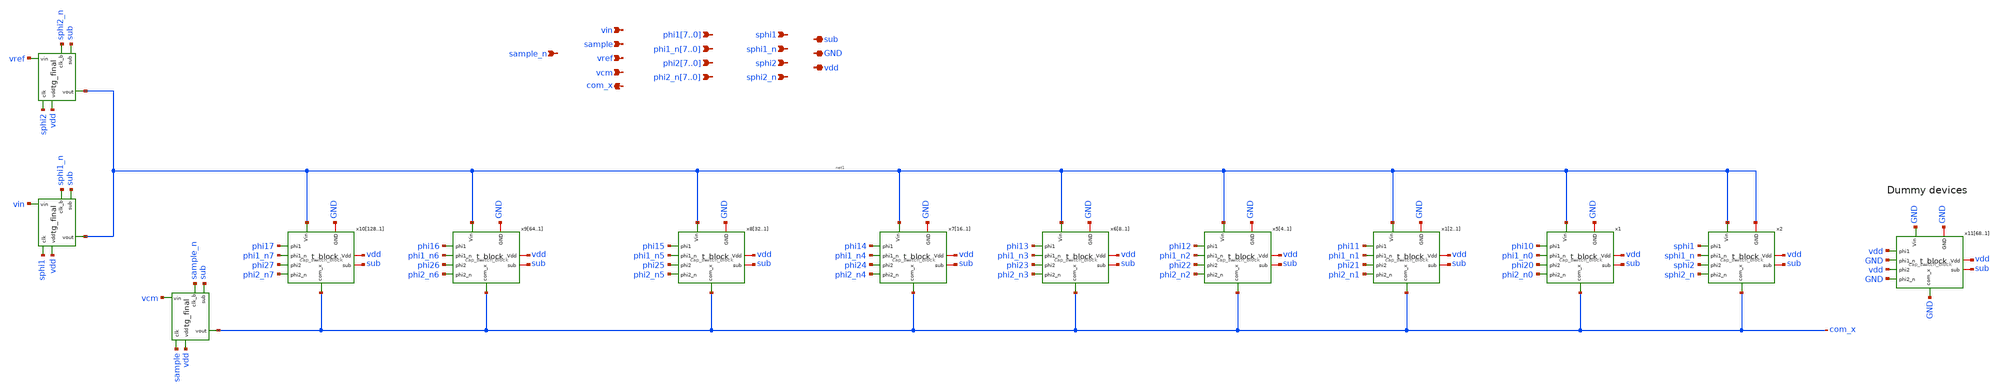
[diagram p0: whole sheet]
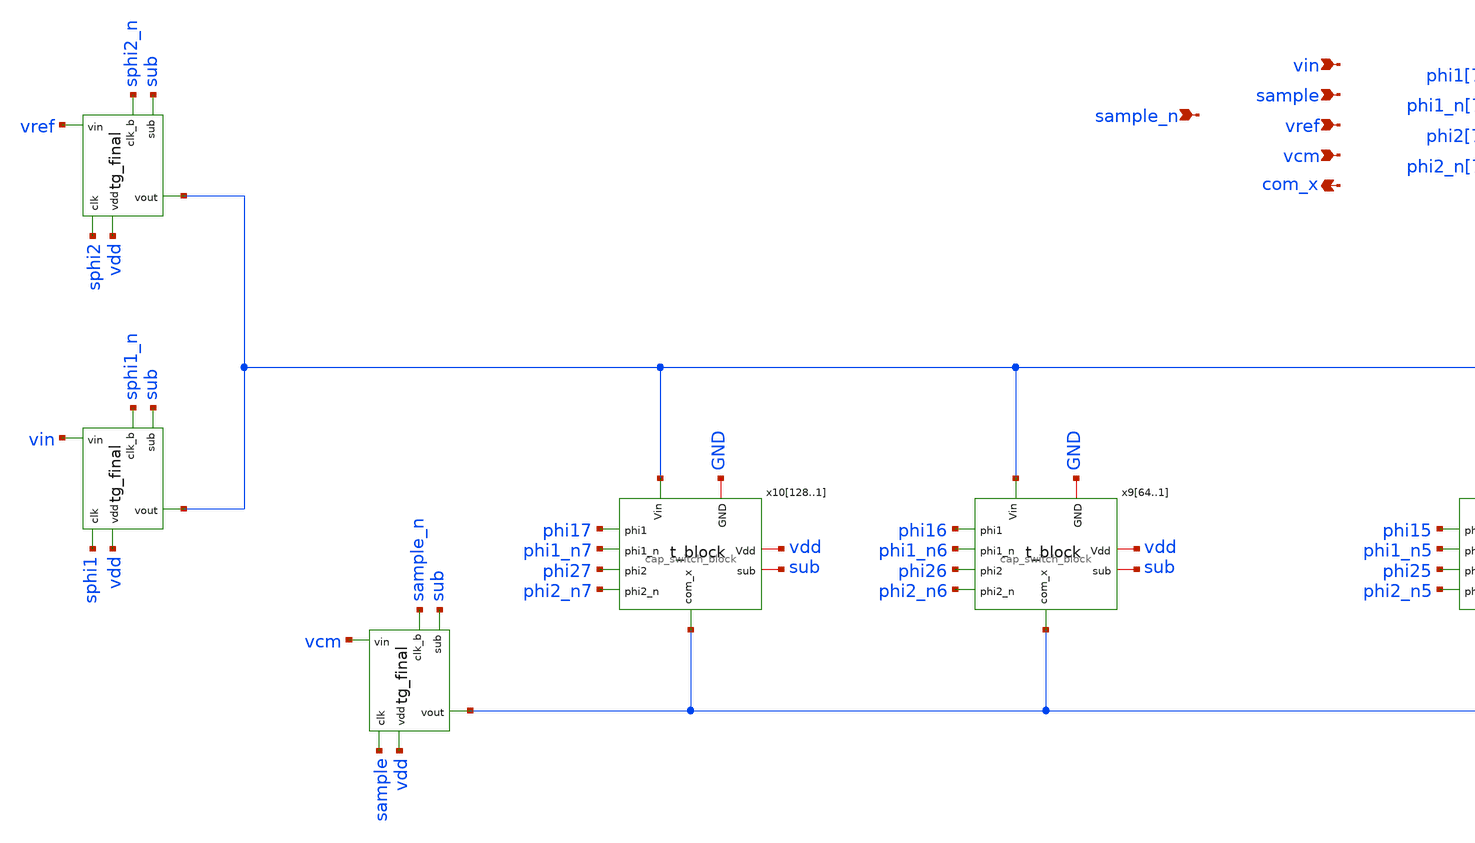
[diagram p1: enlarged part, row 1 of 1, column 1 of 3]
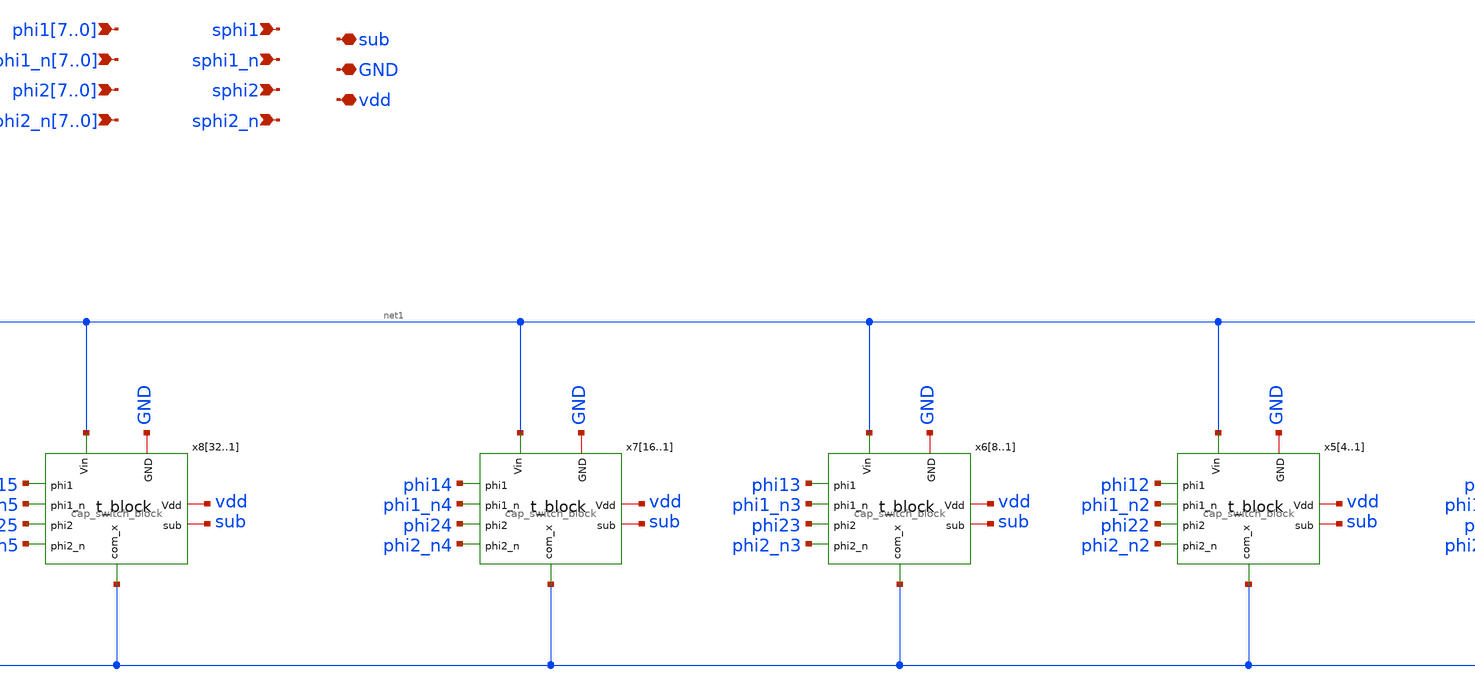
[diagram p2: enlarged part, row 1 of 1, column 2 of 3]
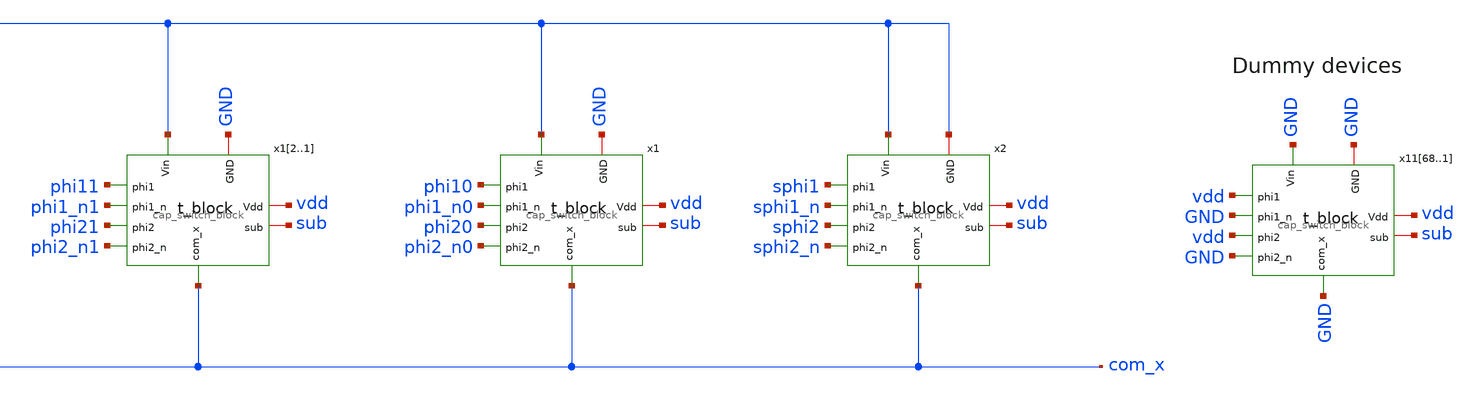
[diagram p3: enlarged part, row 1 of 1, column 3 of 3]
** sch_path: top/test/design/capdac_m.sch
**.subckt capdac_m phi17,phi16,phi15,phi14,phi13,phi12,phi11,phi10
*+ phi1_n7,phi1_n6,phi1_n5,phi1_n4,phi1_n3,phi1_n2,phi1_n1,phi1_n0 vdd GND sub phi27,phi26,phi25,phi24,phi23,phi22,phi21,phi20
*+ phi2_n7,phi2_n6,phi2_n5,phi2_n4,phi2_n3,phi2_n2,phi2_n1,phi2_n0 com_x sphi1 sphi1_n sphi2 sphi2_n vcm vref sample sample_n vin
*.ipin phi17,phi16,phi15,phi14,phi13,phi12,phi11,phi10
*.ipin phi1_n7,phi1_n6,phi1_n5,phi1_n4,phi1_n3,phi1_n2,phi1_n1,phi1_n0
*.iopin vdd
*.iopin GND
*.iopin sub
*.ipin phi27,phi26,phi25,phi24,phi23,phi22,phi21,phi20
*.ipin phi2_n7,phi2_n6,phi2_n5,phi2_n4,phi2_n3,phi2_n2,phi2_n1,phi2_n0
*.opin com_x
*.ipin sphi1
*.ipin sphi1_n
*.ipin sphi2
*.ipin sphi2_n
*.ipin vcm
*.ipin vref
*.ipin sample
*.ipin sample_n
*.ipin vin
x2 net1 sub net1 vdd sphi1 sphi2 sphi2_n sphi1_n com_x cap_switch_block
x1 net1 sub GND vdd phi10 phi20 phi2_n0 phi1_n0 com_x cap_switch_block
x12 net1 sub GND vdd phi11 phi21 phi2_n1 phi1_n1 com_x cap_switch_block
x11 net1 sub GND vdd phi11 phi21 phi2_n1 phi1_n1 com_x cap_switch_block
x54 net1 sub GND vdd phi12 phi22 phi2_n2 phi1_n2 com_x cap_switch_block
x53 net1 sub GND vdd phi12 phi22 phi2_n2 phi1_n2 com_x cap_switch_block
x52 net1 sub GND vdd phi12 phi22 phi2_n2 phi1_n2 com_x cap_switch_block
x51 net1 sub GND vdd phi12 phi22 phi2_n2 phi1_n2 com_x cap_switch_block
x68 net1 sub GND vdd phi13 phi23 phi2_n3 phi1_n3 com_x cap_switch_block
x67 net1 sub GND vdd phi13 phi23 phi2_n3 phi1_n3 com_x cap_switch_block
x66 net1 sub GND vdd phi13 phi23 phi2_n3 phi1_n3 com_x cap_switch_block
x65 net1 sub GND vdd phi13 phi23 phi2_n3 phi1_n3 com_x cap_switch_block
x64 net1 sub GND vdd phi13 phi23 phi2_n3 phi1_n3 com_x cap_switch_block
x63 net1 sub GND vdd phi13 phi23 phi2_n3 phi1_n3 com_x cap_switch_block
x62 net1 sub GND vdd phi13 phi23 phi2_n3 phi1_n3 com_x cap_switch_block
x61 net1 sub GND vdd phi13 phi23 phi2_n3 phi1_n3 com_x cap_switch_block
x716 net1 sub GND vdd phi14 phi24 phi2_n4 phi1_n4 com_x cap_switch_block
x715 net1 sub GND vdd phi14 phi24 phi2_n4 phi1_n4 com_x cap_switch_block
x714 net1 sub GND vdd phi14 phi24 phi2_n4 phi1_n4 com_x cap_switch_block
x713 net1 sub GND vdd phi14 phi24 phi2_n4 phi1_n4 com_x cap_switch_block
x712 net1 sub GND vdd phi14 phi24 phi2_n4 phi1_n4 com_x cap_switch_block
x711 net1 sub GND vdd phi14 phi24 phi2_n4 phi1_n4 com_x cap_switch_block
x710 net1 sub GND vdd phi14 phi24 phi2_n4 phi1_n4 com_x cap_switch_block
x79 net1 sub GND vdd phi14 phi24 phi2_n4 phi1_n4 com_x cap_switch_block
x78 net1 sub GND vdd phi14 phi24 phi2_n4 phi1_n4 com_x cap_switch_block
x77 net1 sub GND vdd phi14 phi24 phi2_n4 phi1_n4 com_x cap_switch_block
x76 net1 sub GND vdd phi14 phi24 phi2_n4 phi1_n4 com_x cap_switch_block
x75 net1 sub GND vdd phi14 phi24 phi2_n4 phi1_n4 com_x cap_switch_block
x74 net1 sub GND vdd phi14 phi24 phi2_n4 phi1_n4 com_x cap_switch_block
x73 net1 sub GND vdd phi14 phi24 phi2_n4 phi1_n4 com_x cap_switch_block
x72 net1 sub GND vdd phi14 phi24 phi2_n4 phi1_n4 com_x cap_switch_block
x71 net1 sub GND vdd phi14 phi24 phi2_n4 phi1_n4 com_x cap_switch_block
x832 net1 sub GND vdd phi15 phi25 phi2_n5 phi1_n5 com_x cap_switch_block
x831 net1 sub GND vdd phi15 phi25 phi2_n5 phi1_n5 com_x cap_switch_block
x830 net1 sub GND vdd phi15 phi25 phi2_n5 phi1_n5 com_x cap_switch_block
x829 net1 sub GND vdd phi15 phi25 phi2_n5 phi1_n5 com_x cap_switch_block
x828 net1 sub GND vdd phi15 phi25 phi2_n5 phi1_n5 com_x cap_switch_block
x827 net1 sub GND vdd phi15 phi25 phi2_n5 phi1_n5 com_x cap_switch_block
x826 net1 sub GND vdd phi15 phi25 phi2_n5 phi1_n5 com_x cap_switch_block
x825 net1 sub GND vdd phi15 phi25 phi2_n5 phi1_n5 com_x cap_switch_block
x824 net1 sub GND vdd phi15 phi25 phi2_n5 phi1_n5 com_x cap_switch_block
x823 net1 sub GND vdd phi15 phi25 phi2_n5 phi1_n5 com_x cap_switch_block
x822 net1 sub GND vdd phi15 phi25 phi2_n5 phi1_n5 com_x cap_switch_block
x821 net1 sub GND vdd phi15 phi25 phi2_n5 phi1_n5 com_x cap_switch_block
x820 net1 sub GND vdd phi15 phi25 phi2_n5 phi1_n5 com_x cap_switch_block
x819 net1 sub GND vdd phi15 phi25 phi2_n5 phi1_n5 com_x cap_switch_block
x818 net1 sub GND vdd phi15 phi25 phi2_n5 phi1_n5 com_x cap_switch_block
x817 net1 sub GND vdd phi15 phi25 phi2_n5 phi1_n5 com_x cap_switch_block
x816 net1 sub GND vdd phi15 phi25 phi2_n5 phi1_n5 com_x cap_switch_block
x815 net1 sub GND vdd phi15 phi25 phi2_n5 phi1_n5 com_x cap_switch_block
x814 net1 sub GND vdd phi15 phi25 phi2_n5 phi1_n5 com_x cap_switch_block
x813 net1 sub GND vdd phi15 phi25 phi2_n5 phi1_n5 com_x cap_switch_block
x812 net1 sub GND vdd phi15 phi25 phi2_n5 phi1_n5 com_x cap_switch_block
x811 net1 sub GND vdd phi15 phi25 phi2_n5 phi1_n5 com_x cap_switch_block
x810 net1 sub GND vdd phi15 phi25 phi2_n5 phi1_n5 com_x cap_switch_block
x89 net1 sub GND vdd phi15 phi25 phi2_n5 phi1_n5 com_x cap_switch_block
x88 net1 sub GND vdd phi15 phi25 phi2_n5 phi1_n5 com_x cap_switch_block
x87 net1 sub GND vdd phi15 phi25 phi2_n5 phi1_n5 com_x cap_switch_block
x86 net1 sub GND vdd phi15 phi25 phi2_n5 phi1_n5 com_x cap_switch_block
x85 net1 sub GND vdd phi15 phi25 phi2_n5 phi1_n5 com_x cap_switch_block
x84 net1 sub GND vdd phi15 phi25 phi2_n5 phi1_n5 com_x cap_switch_block
x83 net1 sub GND vdd phi15 phi25 phi2_n5 phi1_n5 com_x cap_switch_block
x82 net1 sub GND vdd phi15 phi25 phi2_n5 phi1_n5 com_x cap_switch_block
x81 net1 sub GND vdd phi15 phi25 phi2_n5 phi1_n5 com_x cap_switch_block
x964 net1 sub GND vdd phi16 phi26 phi2_n6 phi1_n6 com_x cap_switch_block
x963 net1 sub GND vdd phi16 phi26 phi2_n6 phi1_n6 com_x cap_switch_block
x962 net1 sub GND vdd phi16 phi26 phi2_n6 phi1_n6 com_x cap_switch_block
x961 net1 sub GND vdd phi16 phi26 phi2_n6 phi1_n6 com_x cap_switch_block
x960 net1 sub GND vdd phi16 phi26 phi2_n6 phi1_n6 com_x cap_switch_block
x959 net1 sub GND vdd phi16 phi26 phi2_n6 phi1_n6 com_x cap_switch_block
x958 net1 sub GND vdd phi16 phi26 phi2_n6 phi1_n6 com_x cap_switch_block
x957 net1 sub GND vdd phi16 phi26 phi2_n6 phi1_n6 com_x cap_switch_block
x956 net1 sub GND vdd phi16 phi26 phi2_n6 phi1_n6 com_x cap_switch_block
x955 net1 sub GND vdd phi16 phi26 phi2_n6 phi1_n6 com_x cap_switch_block
x954 net1 sub GND vdd phi16 phi26 phi2_n6 phi1_n6 com_x cap_switch_block
x953 net1 sub GND vdd phi16 phi26 phi2_n6 phi1_n6 com_x cap_switch_block
x952 net1 sub GND vdd phi16 phi26 phi2_n6 phi1_n6 com_x cap_switch_block
x951 net1 sub GND vdd phi16 phi26 phi2_n6 phi1_n6 com_x cap_switch_block
x950 net1 sub GND vdd phi16 phi26 phi2_n6 phi1_n6 com_x cap_switch_block
x949 net1 sub GND vdd phi16 phi26 phi2_n6 phi1_n6 com_x cap_switch_block
x948 net1 sub GND vdd phi16 phi26 phi2_n6 phi1_n6 com_x cap_switch_block
x947 net1 sub GND vdd phi16 phi26 phi2_n6 phi1_n6 com_x cap_switch_block
x946 net1 sub GND vdd phi16 phi26 phi2_n6 phi1_n6 com_x cap_switch_block
x945 net1 sub GND vdd phi16 phi26 phi2_n6 phi1_n6 com_x cap_switch_block
x944 net1 sub GND vdd phi16 phi26 phi2_n6 phi1_n6 com_x cap_switch_block
x943 net1 sub GND vdd phi16 phi26 phi2_n6 phi1_n6 com_x cap_switch_block
x942 net1 sub GND vdd phi16 phi26 phi2_n6 phi1_n6 com_x cap_switch_block
x941 net1 sub GND vdd phi16 phi26 phi2_n6 phi1_n6 com_x cap_switch_block
x940 net1 sub GND vdd phi16 phi26 phi2_n6 phi1_n6 com_x cap_switch_block
x939 net1 sub GND vdd phi16 phi26 phi2_n6 phi1_n6 com_x cap_switch_block
x938 net1 sub GND vdd phi16 phi26 phi2_n6 phi1_n6 com_x cap_switch_block
x937 net1 sub GND vdd phi16 phi26 phi2_n6 phi1_n6 com_x cap_switch_block
x936 net1 sub GND vdd phi16 phi26 phi2_n6 phi1_n6 com_x cap_switch_block
x935 net1 sub GND vdd phi16 phi26 phi2_n6 phi1_n6 com_x cap_switch_block
x934 net1 sub GND vdd phi16 phi26 phi2_n6 phi1_n6 com_x cap_switch_block
x933 net1 sub GND vdd phi16 phi26 phi2_n6 phi1_n6 com_x cap_switch_block
x932 net1 sub GND vdd phi16 phi26 phi2_n6 phi1_n6 com_x cap_switch_block
x931 net1 sub GND vdd phi16 phi26 phi2_n6 phi1_n6 com_x cap_switch_block
x930 net1 sub GND vdd phi16 phi26 phi2_n6 phi1_n6 com_x cap_switch_block
x929 net1 sub GND vdd phi16 phi26 phi2_n6 phi1_n6 com_x cap_switch_block
x928 net1 sub GND vdd phi16 phi26 phi2_n6 phi1_n6 com_x cap_switch_block
x927 net1 sub GND vdd phi16 phi26 phi2_n6 phi1_n6 com_x cap_switch_block
x926 net1 sub GND vdd phi16 phi26 phi2_n6 phi1_n6 com_x cap_switch_block
x925 net1 sub GND vdd phi16 phi26 phi2_n6 phi1_n6 com_x cap_switch_block
x924 net1 sub GND vdd phi16 phi26 phi2_n6 phi1_n6 com_x cap_switch_block
x923 net1 sub GND vdd phi16 phi26 phi2_n6 phi1_n6 com_x cap_switch_block
x922 net1 sub GND vdd phi16 phi26 phi2_n6 phi1_n6 com_x cap_switch_block
x921 net1 sub GND vdd phi16 phi26 phi2_n6 phi1_n6 com_x cap_switch_block
x920 net1 sub GND vdd phi16 phi26 phi2_n6 phi1_n6 com_x cap_switch_block
x919 net1 sub GND vdd phi16 phi26 phi2_n6 phi1_n6 com_x cap_switch_block
x918 net1 sub GND vdd phi16 phi26 phi2_n6 phi1_n6 com_x cap_switch_block
x917 net1 sub GND vdd phi16 phi26 phi2_n6 phi1_n6 com_x cap_switch_block
x916 net1 sub GND vdd phi16 phi26 phi2_n6 phi1_n6 com_x cap_switch_block
x915 net1 sub GND vdd phi16 phi26 phi2_n6 phi1_n6 com_x cap_switch_block
x914 net1 sub GND vdd phi16 phi26 phi2_n6 phi1_n6 com_x cap_switch_block
x913 net1 sub GND vdd phi16 phi26 phi2_n6 phi1_n6 com_x cap_switch_block
x912 net1 sub GND vdd phi16 phi26 phi2_n6 phi1_n6 com_x cap_switch_block
x911 net1 sub GND vdd phi16 phi26 phi2_n6 phi1_n6 com_x cap_switch_block
x910 net1 sub GND vdd phi16 phi26 phi2_n6 phi1_n6 com_x cap_switch_block
x99 net1 sub GND vdd phi16 phi26 phi2_n6 phi1_n6 com_x cap_switch_block
x98 net1 sub GND vdd phi16 phi26 phi2_n6 phi1_n6 com_x cap_switch_block
x97 net1 sub GND vdd phi16 phi26 phi2_n6 phi1_n6 com_x cap_switch_block
x96 net1 sub GND vdd phi16 phi26 phi2_n6 phi1_n6 com_x cap_switch_block
x95 net1 sub GND vdd phi16 phi26 phi2_n6 phi1_n6 com_x cap_switch_block
x94 net1 sub GND vdd phi16 phi26 phi2_n6 phi1_n6 com_x cap_switch_block
x93 net1 sub GND vdd phi16 phi26 phi2_n6 phi1_n6 com_x cap_switch_block
x92 net1 sub GND vdd phi16 phi26 phi2_n6 phi1_n6 com_x cap_switch_block
x91 net1 sub GND vdd phi16 phi26 phi2_n6 phi1_n6 com_x cap_switch_block
x10128 net1 sub GND vdd phi17 phi27 phi2_n7 phi1_n7 com_x cap_switch_block
x10127 net1 sub GND vdd phi17 phi27 phi2_n7 phi1_n7 com_x cap_switch_block
x10126 net1 sub GND vdd phi17 phi27 phi2_n7 phi1_n7 com_x cap_switch_block
x10125 net1 sub GND vdd phi17 phi27 phi2_n7 phi1_n7 com_x cap_switch_block
x10124 net1 sub GND vdd phi17 phi27 phi2_n7 phi1_n7 com_x cap_switch_block
x10123 net1 sub GND vdd phi17 phi27 phi2_n7 phi1_n7 com_x cap_switch_block
x10122 net1 sub GND vdd phi17 phi27 phi2_n7 phi1_n7 com_x cap_switch_block
x10121 net1 sub GND vdd phi17 phi27 phi2_n7 phi1_n7 com_x cap_switch_block
x10120 net1 sub GND vdd phi17 phi27 phi2_n7 phi1_n7 com_x cap_switch_block
x10119 net1 sub GND vdd phi17 phi27 phi2_n7 phi1_n7 com_x cap_switch_block
x10118 net1 sub GND vdd phi17 phi27 phi2_n7 phi1_n7 com_x cap_switch_block
x10117 net1 sub GND vdd phi17 phi27 phi2_n7 phi1_n7 com_x cap_switch_block
x10116 net1 sub GND vdd phi17 phi27 phi2_n7 phi1_n7 com_x cap_switch_block
x10115 net1 sub GND vdd phi17 phi27 phi2_n7 phi1_n7 com_x cap_switch_block
x10114 net1 sub GND vdd phi17 phi27 phi2_n7 phi1_n7 com_x cap_switch_block
x10113 net1 sub GND vdd phi17 phi27 phi2_n7 phi1_n7 com_x cap_switch_block
x10112 net1 sub GND vdd phi17 phi27 phi2_n7 phi1_n7 com_x cap_switch_block
x10111 net1 sub GND vdd phi17 phi27 phi2_n7 phi1_n7 com_x cap_switch_block
x10110 net1 sub GND vdd phi17 phi27 phi2_n7 phi1_n7 com_x cap_switch_block
x10109 net1 sub GND vdd phi17 phi27 phi2_n7 phi1_n7 com_x cap_switch_block
x10108 net1 sub GND vdd phi17 phi27 phi2_n7 phi1_n7 com_x cap_switch_block
x10107 net1 sub GND vdd phi17 phi27 phi2_n7 phi1_n7 com_x cap_switch_block
x10106 net1 sub GND vdd phi17 phi27 phi2_n7 phi1_n7 com_x cap_switch_block
x10105 net1 sub GND vdd phi17 phi27 phi2_n7 phi1_n7 com_x cap_switch_block
x10104 net1 sub GND vdd phi17 phi27 phi2_n7 phi1_n7 com_x cap_switch_block
x10103 net1 sub GND vdd phi17 phi27 phi2_n7 phi1_n7 com_x cap_switch_block
x10102 net1 sub GND vdd phi17 phi27 phi2_n7 phi1_n7 com_x cap_switch_block
x10101 net1 sub GND vdd phi17 phi27 phi2_n7 phi1_n7 com_x cap_switch_block
x10100 net1 sub GND vdd phi17 phi27 phi2_n7 phi1_n7 com_x cap_switch_block
x1099 net1 sub GND vdd phi17 phi27 phi2_n7 phi1_n7 com_x cap_switch_block
x1098 net1 sub GND vdd phi17 phi27 phi2_n7 phi1_n7 com_x cap_switch_block
x1097 net1 sub GND vdd phi17 phi27 phi2_n7 phi1_n7 com_x cap_switch_block
x1096 net1 sub GND vdd phi17 phi27 phi2_n7 phi1_n7 com_x cap_switch_block
x1095 net1 sub GND vdd phi17 phi27 phi2_n7 phi1_n7 com_x cap_switch_block
x1094 net1 sub GND vdd phi17 phi27 phi2_n7 phi1_n7 com_x cap_switch_block
x1093 net1 sub GND vdd phi17 phi27 phi2_n7 phi1_n7 com_x cap_switch_block
x1092 net1 sub GND vdd phi17 phi27 phi2_n7 phi1_n7 com_x cap_switch_block
x1091 net1 sub GND vdd phi17 phi27 phi2_n7 phi1_n7 com_x cap_switch_block
x1090 net1 sub GND vdd phi17 phi27 phi2_n7 phi1_n7 com_x cap_switch_block
x1089 net1 sub GND vdd phi17 phi27 phi2_n7 phi1_n7 com_x cap_switch_block
x1088 net1 sub GND vdd phi17 phi27 phi2_n7 phi1_n7 com_x cap_switch_block
x1087 net1 sub GND vdd phi17 phi27 phi2_n7 phi1_n7 com_x cap_switch_block
x1086 net1 sub GND vdd phi17 phi27 phi2_n7 phi1_n7 com_x cap_switch_block
x1085 net1 sub GND vdd phi17 phi27 phi2_n7 phi1_n7 com_x cap_switch_block
x1084 net1 sub GND vdd phi17 phi27 phi2_n7 phi1_n7 com_x cap_switch_block
x1083 net1 sub GND vdd phi17 phi27 phi2_n7 phi1_n7 com_x cap_switch_block
x1082 net1 sub GND vdd phi17 phi27 phi2_n7 phi1_n7 com_x cap_switch_block
x1081 net1 sub GND vdd phi17 phi27 phi2_n7 phi1_n7 com_x cap_switch_block
x1080 net1 sub GND vdd phi17 phi27 phi2_n7 phi1_n7 com_x cap_switch_block
x1079 net1 sub GND vdd phi17 phi27 phi2_n7 phi1_n7 com_x cap_switch_block
x1078 net1 sub GND vdd phi17 phi27 phi2_n7 phi1_n7 com_x cap_switch_block
x1077 net1 sub GND vdd phi17 phi27 phi2_n7 phi1_n7 com_x cap_switch_block
x1076 net1 sub GND vdd phi17 phi27 phi2_n7 phi1_n7 com_x cap_switch_block
x1075 net1 sub GND vdd phi17 phi27 phi2_n7 phi1_n7 com_x cap_switch_block
x1074 net1 sub GND vdd phi17 phi27 phi2_n7 phi1_n7 com_x cap_switch_block
x1073 net1 sub GND vdd phi17 phi27 phi2_n7 phi1_n7 com_x cap_switch_block
x1072 net1 sub GND vdd phi17 phi27 phi2_n7 phi1_n7 com_x cap_switch_block
x1071 net1 sub GND vdd phi17 phi27 phi2_n7 phi1_n7 com_x cap_switch_block
x1070 net1 sub GND vdd phi17 phi27 phi2_n7 phi1_n7 com_x cap_switch_block
x1069 net1 sub GND vdd phi17 phi27 phi2_n7 phi1_n7 com_x cap_switch_block
x1068 net1 sub GND vdd phi17 phi27 phi2_n7 phi1_n7 com_x cap_switch_block
x1067 net1 sub GND vdd phi17 phi27 phi2_n7 phi1_n7 com_x cap_switch_block
x1066 net1 sub GND vdd phi17 phi27 phi2_n7 phi1_n7 com_x cap_switch_block
x1065 net1 sub GND vdd phi17 phi27 phi2_n7 phi1_n7 com_x cap_switch_block
x1064 net1 sub GND vdd phi17 phi27 phi2_n7 phi1_n7 com_x cap_switch_block
x1063 net1 sub GND vdd phi17 phi27 phi2_n7 phi1_n7 com_x cap_switch_block
x1062 net1 sub GND vdd phi17 phi27 phi2_n7 phi1_n7 com_x cap_switch_block
x1061 net1 sub GND vdd phi17 phi27 phi2_n7 phi1_n7 com_x cap_switch_block
x1060 net1 sub GND vdd phi17 phi27 phi2_n7 phi1_n7 com_x cap_switch_block
x1059 net1 sub GND vdd phi17 phi27 phi2_n7 phi1_n7 com_x cap_switch_block
x1058 net1 sub GND vdd phi17 phi27 phi2_n7 phi1_n7 com_x cap_switch_block
x1057 net1 sub GND vdd phi17 phi27 phi2_n7 phi1_n7 com_x cap_switch_block
x1056 net1 sub GND vdd phi17 phi27 phi2_n7 phi1_n7 com_x cap_switch_block
x1055 net1 sub GND vdd phi17 phi27 phi2_n7 phi1_n7 com_x cap_switch_block
x1054 net1 sub GND vdd phi17 phi27 phi2_n7 phi1_n7 com_x cap_switch_block
x1053 net1 sub GND vdd phi17 phi27 phi2_n7 phi1_n7 com_x cap_switch_block
x1052 net1 sub GND vdd phi17 phi27 phi2_n7 phi1_n7 com_x cap_switch_block
x1051 net1 sub GND vdd phi17 phi27 phi2_n7 phi1_n7 com_x cap_switch_block
x1050 net1 sub GND vdd phi17 phi27 phi2_n7 phi1_n7 com_x cap_switch_block
x1049 net1 sub GND vdd phi17 phi27 phi2_n7 phi1_n7 com_x cap_switch_block
x1048 net1 sub GND vdd phi17 phi27 phi2_n7 phi1_n7 com_x cap_switch_block
x1047 net1 sub GND vdd phi17 phi27 phi2_n7 phi1_n7 com_x cap_switch_block
x1046 net1 sub GND vdd phi17 phi27 phi2_n7 phi1_n7 com_x cap_switch_block
x1045 net1 sub GND vdd phi17 phi27 phi2_n7 phi1_n7 com_x cap_switch_block
x1044 net1 sub GND vdd phi17 phi27 phi2_n7 phi1_n7 com_x cap_switch_block
x1043 net1 sub GND vdd phi17 phi27 phi2_n7 phi1_n7 com_x cap_switch_block
x1042 net1 sub GND vdd phi17 phi27 phi2_n7 phi1_n7 com_x cap_switch_block
x1041 net1 sub GND vdd phi17 phi27 phi2_n7 phi1_n7 com_x cap_switch_block
x1040 net1 sub GND vdd phi17 phi27 phi2_n7 phi1_n7 com_x cap_switch_block
x1039 net1 sub GND vdd phi17 phi27 phi2_n7 phi1_n7 com_x cap_switch_block
x1038 net1 sub GND vdd phi17 phi27 phi2_n7 phi1_n7 com_x cap_switch_block
x1037 net1 sub GND vdd phi17 phi27 phi2_n7 phi1_n7 com_x cap_switch_block
x1036 net1 sub GND vdd phi17 phi27 phi2_n7 phi1_n7 com_x cap_switch_block
x1035 net1 sub GND vdd phi17 phi27 phi2_n7 phi1_n7 com_x cap_switch_block
x1034 net1 sub GND vdd phi17 phi27 phi2_n7 phi1_n7 com_x cap_switch_block
x1033 net1 sub GND vdd phi17 phi27 phi2_n7 phi1_n7 com_x cap_switch_block
x1032 net1 sub GND vdd phi17 phi27 phi2_n7 phi1_n7 com_x cap_switch_block
x1031 net1 sub GND vdd phi17 phi27 phi2_n7 phi1_n7 com_x cap_switch_block
x1030 net1 sub GND vdd phi17 phi27 phi2_n7 phi1_n7 com_x cap_switch_block
x1029 net1 sub GND vdd phi17 phi27 phi2_n7 phi1_n7 com_x cap_switch_block
x1028 net1 sub GND vdd phi17 phi27 phi2_n7 phi1_n7 com_x cap_switch_block
x1027 net1 sub GND vdd phi17 phi27 phi2_n7 phi1_n7 com_x cap_switch_block
x1026 net1 sub GND vdd phi17 phi27 phi2_n7 phi1_n7 com_x cap_switch_block
x1025 net1 sub GND vdd phi17 phi27 phi2_n7 phi1_n7 com_x cap_switch_block
x1024 net1 sub GND vdd phi17 phi27 phi2_n7 phi1_n7 com_x cap_switch_block
x1023 net1 sub GND vdd phi17 phi27 phi2_n7 phi1_n7 com_x cap_switch_block
x1022 net1 sub GND vdd phi17 phi27 phi2_n7 phi1_n7 com_x cap_switch_block
x1021 net1 sub GND vdd phi17 phi27 phi2_n7 phi1_n7 com_x cap_switch_block
x1020 net1 sub GND vdd phi17 phi27 phi2_n7 phi1_n7 com_x cap_switch_block
x1019 net1 sub GND vdd phi17 phi27 phi2_n7 phi1_n7 com_x cap_switch_block
x1018 net1 sub GND vdd phi17 phi27 phi2_n7 phi1_n7 com_x cap_switch_block
x1017 net1 sub GND vdd phi17 phi27 phi2_n7 phi1_n7 com_x cap_switch_block
x1016 net1 sub GND vdd phi17 phi27 phi2_n7 phi1_n7 com_x cap_switch_block
x1015 net1 sub GND vdd phi17 phi27 phi2_n7 phi1_n7 com_x cap_switch_block
x1014 net1 sub GND vdd phi17 phi27 phi2_n7 phi1_n7 com_x cap_switch_block
x1013 net1 sub GND vdd phi17 phi27 phi2_n7 phi1_n7 com_x cap_switch_block
x1012 net1 sub GND vdd phi17 phi27 phi2_n7 phi1_n7 com_x cap_switch_block
x1011 net1 sub GND vdd phi17 phi27 phi2_n7 phi1_n7 com_x cap_switch_block
x1010 net1 sub GND vdd phi17 phi27 phi2_n7 phi1_n7 com_x cap_switch_block
x109 net1 sub GND vdd phi17 phi27 phi2_n7 phi1_n7 com_x cap_switch_block
x108 net1 sub GND vdd phi17 phi27 phi2_n7 phi1_n7 com_x cap_switch_block
x107 net1 sub GND vdd phi17 phi27 phi2_n7 phi1_n7 com_x cap_switch_block
x106 net1 sub GND vdd phi17 phi27 phi2_n7 phi1_n7 com_x cap_switch_block
x105 net1 sub GND vdd phi17 phi27 phi2_n7 phi1_n7 com_x cap_switch_block
x104 net1 sub GND vdd phi17 phi27 phi2_n7 phi1_n7 com_x cap_switch_block
x103 net1 sub GND vdd phi17 phi27 phi2_n7 phi1_n7 com_x cap_switch_block
x102 net1 sub GND vdd phi17 phi27 phi2_n7 phi1_n7 com_x cap_switch_block
x101 net1 sub GND vdd phi17 phi27 phi2_n7 phi1_n7 com_x cap_switch_block
x410 sphi2 sub net1 vref vdd sphi2_n tg_final
x49 sphi2 sub net1 vref vdd sphi2_n tg_final
x48 sphi2 sub net1 vref vdd sphi2_n tg_final
x47 sphi2 sub net1 vref vdd sphi2_n tg_final
x46 sphi2 sub net1 vref vdd sphi2_n tg_final
x45 sphi2 sub net1 vref vdd sphi2_n tg_final
x44 sphi2 sub net1 vref vdd sphi2_n tg_final
x43 sphi2 sub net1 vref vdd sphi2_n tg_final
x42 sphi2 sub net1 vref vdd sphi2_n tg_final
x41 sphi2 sub net1 vref vdd sphi2_n tg_final
x210 sphi1 sub net1 vin vdd sphi1_n tg_final
x29 sphi1 sub net1 vin vdd sphi1_n tg_final
x28 sphi1 sub net1 vin vdd sphi1_n tg_final
x27 sphi1 sub net1 vin vdd sphi1_n tg_final
x26 sphi1 sub net1 vin vdd sphi1_n tg_final
x25 sphi1 sub net1 vin vdd sphi1_n tg_final
x24 sphi1 sub net1 vin vdd sphi1_n tg_final
x23 sphi1 sub net1 vin vdd sphi1_n tg_final
x22 sphi1 sub net1 vin vdd sphi1_n tg_final
x21 sphi1 sub net1 vin vdd sphi1_n tg_final
x310 sample sub com_x vcm vdd sample_n tg_final
x39 sample sub com_x vcm vdd sample_n tg_final
x38 sample sub com_x vcm vdd sample_n tg_final
x37 sample sub com_x vcm vdd sample_n tg_final
x36 sample sub com_x vcm vdd sample_n tg_final
x35 sample sub com_x vcm vdd sample_n tg_final
x34 sample sub com_x vcm vdd sample_n tg_final
x33 sample sub com_x vcm vdd sample_n tg_final
x32 sample sub com_x vcm vdd sample_n tg_final
x31 sample sub com_x vcm vdd sample_n tg_final
x1168 GND sub GND vdd vdd vdd GND GND GND cap_switch_block
x1167 GND sub GND vdd vdd vdd GND GND GND cap_switch_block
x1166 GND sub GND vdd vdd vdd GND GND GND cap_switch_block
x1165 GND sub GND vdd vdd vdd GND GND GND cap_switch_block
x1164 GND sub GND vdd vdd vdd GND GND GND cap_switch_block
x1163 GND sub GND vdd vdd vdd GND GND GND cap_switch_block
x1162 GND sub GND vdd vdd vdd GND GND GND cap_switch_block
x1161 GND sub GND vdd vdd vdd GND GND GND cap_switch_block
x1160 GND sub GND vdd vdd vdd GND GND GND cap_switch_block
x1159 GND sub GND vdd vdd vdd GND GND GND cap_switch_block
x1158 GND sub GND vdd vdd vdd GND GND GND cap_switch_block
x1157 GND sub GND vdd vdd vdd GND GND GND cap_switch_block
x1156 GND sub GND vdd vdd vdd GND GND GND cap_switch_block
x1155 GND sub GND vdd vdd vdd GND GND GND cap_switch_block
x1154 GND sub GND vdd vdd vdd GND GND GND cap_switch_block
x1153 GND sub GND vdd vdd vdd GND GND GND cap_switch_block
x1152 GND sub GND vdd vdd vdd GND GND GND cap_switch_block
x1151 GND sub GND vdd vdd vdd GND GND GND cap_switch_block
x1150 GND sub GND vdd vdd vdd GND GND GND cap_switch_block
x1149 GND sub GND vdd vdd vdd GND GND GND cap_switch_block
x1148 GND sub GND vdd vdd vdd GND GND GND cap_switch_block
x1147 GND sub GND vdd vdd vdd GND GND GND cap_switch_block
x1146 GND sub GND vdd vdd vdd GND GND GND cap_switch_block
x1145 GND sub GND vdd vdd vdd GND GND GND cap_switch_block
x1144 GND sub GND vdd vdd vdd GND GND GND cap_switch_block
x1143 GND sub GND vdd vdd vdd GND GND GND cap_switch_block
x1142 GND sub GND vdd vdd vdd GND GND GND cap_switch_block
x1141 GND sub GND vdd vdd vdd GND GND GND cap_switch_block
x1140 GND sub GND vdd vdd vdd GND GND GND cap_switch_block
x1139 GND sub GND vdd vdd vdd GND GND GND cap_switch_block
x1138 GND sub GND vdd vdd vdd GND GND GND cap_switch_block
x1137 GND sub GND vdd vdd vdd GND GND GND cap_switch_block
x1136 GND sub GND vdd vdd vdd GND GND GND cap_switch_block
x1135 GND sub GND vdd vdd vdd GND GND GND cap_switch_block
x1134 GND sub GND vdd vdd vdd GND GND GND cap_switch_block
x1133 GND sub GND vdd vdd vdd GND GND GND cap_switch_block
x1132 GND sub GND vdd vdd vdd GND GND GND cap_switch_block
x1131 GND sub GND vdd vdd vdd GND GND GND cap_switch_block
x1130 GND sub GND vdd vdd vdd GND GND GND cap_switch_block
x1129 GND sub GND vdd vdd vdd GND GND GND cap_switch_block
x1128 GND sub GND vdd vdd vdd GND GND GND cap_switch_block
x1127 GND sub GND vdd vdd vdd GND GND GND cap_switch_block
x1126 GND sub GND vdd vdd vdd GND GND GND cap_switch_block
x1125 GND sub GND vdd vdd vdd GND GND GND cap_switch_block
x1124 GND sub GND vdd vdd vdd GND GND GND cap_switch_block
x1123 GND sub GND vdd vdd vdd GND GND GND cap_switch_block
x1122 GND sub GND vdd vdd vdd GND GND GND cap_switch_block
x1121 GND sub GND vdd vdd vdd GND GND GND cap_switch_block
x1120 GND sub GND vdd vdd vdd GND GND GND cap_switch_block
x1119 GND sub GND vdd vdd vdd GND GND GND cap_switch_block
x1118 GND sub GND vdd vdd vdd GND GND GND cap_switch_block
x1117 GND sub GND vdd vdd vdd GND GND GND cap_switch_block
x1116 GND sub GND vdd vdd vdd GND GND GND cap_switch_block
x1115 GND sub GND vdd vdd vdd GND GND GND cap_switch_block
x1114 GND sub GND vdd vdd vdd GND GND GND cap_switch_block
x1113 GND sub GND vdd vdd vdd GND GND GND cap_switch_block
x1112 GND sub GND vdd vdd vdd GND GND GND cap_switch_block
x1111 GND sub GND vdd vdd vdd GND GND GND cap_switch_block
x1110 GND sub GND vdd vdd vdd GND GND GND cap_switch_block
x119 GND sub GND vdd vdd vdd GND GND GND cap_switch_block
x118 GND sub GND vdd vdd vdd GND GND GND cap_switch_block
x117 GND sub GND vdd vdd vdd GND GND GND cap_switch_block
x116 GND sub GND vdd vdd vdd GND GND GND cap_switch_block
x115 GND sub GND vdd vdd vdd GND GND GND cap_switch_block
x114 GND sub GND vdd vdd vdd GND GND GND cap_switch_block
x113 GND sub GND vdd vdd vdd GND GND GND cap_switch_block
x112 GND sub GND vdd vdd vdd GND GND GND cap_switch_block
x111 GND sub GND vdd vdd vdd GND GND GND cap_switch_block
**.ends

* expanding   symbol:  /foss/designs/test/design/cap_switch_block.sym # of pins=9
** sym_path: test/design/cap_switch_block.sym
** sch_path: test/design/cap_switch_block.sch
.subckt cap_switch_block Vin sub GND Vdd phi1 phi2 phi2_n phi1_n com_x
*.ipin Vin
*.opin com_x
*.ipin phi1
*.ipin phi1_n
*.iopin Vdd
*.iopin GND
*.iopin sub
*.ipin phi2
*.ipin phi2_n
XC9 com_x net1 sky130_fd_pr__cap_mim_m3_1 W=7 L=7 MF=1 m=1
x4 phi1 sub net1 Vin Vdd phi1_n tg_final
x1 phi2 sub net1 GND Vdd phi2_n tg_final
.ends


* expanding   symbol:  /foss/designs/test/design/tg_final.sym # of pins=6
** sym_path: top/test/design/tg_final.sym
** sch_path: top/test/design/tg_final.sch
.subckt tg_final clk sub vout vin vdd clk_b
*.ipin clk
*.ipin vin
*.opin vout
*.ipin vdd
*.ipin sub
*.ipin clk_b
XM2 vout clk vin sub sky130_fd_pr__nfet_01v8 L=0.15 W=1 nf=1 ad='int((nf+1)/2) * W/nf * 0.29' as='int((nf+2)/2) * W/nf * 0.29'
+ pd='2*int((nf+1)/2) * (W/nf + 0.29)' ps='2*int((nf+2)/2) * (W/nf + 0.29)' nrd='0.29 / W' nrs='0.29 / W'
+ sa=0 sb=0 sd=0 mult=1 m=1
XM1 vout clk_b vin vdd sky130_fd_pr__pfet_01v8 L=0.15 W=1 nf=1 ad='int((nf+1)/2) * W/nf * 0.29' as='int((nf+2)/2) * W/nf * 0.29'
+ pd='2*int((nf+1)/2) * (W/nf + 0.29)' ps='2*int((nf+2)/2) * (W/nf + 0.29)' nrd='0.29 / W' nrs='0.29 / W'
+ sa=0 sb=0 sd=0 mult=1 m=1
.ends

.end
